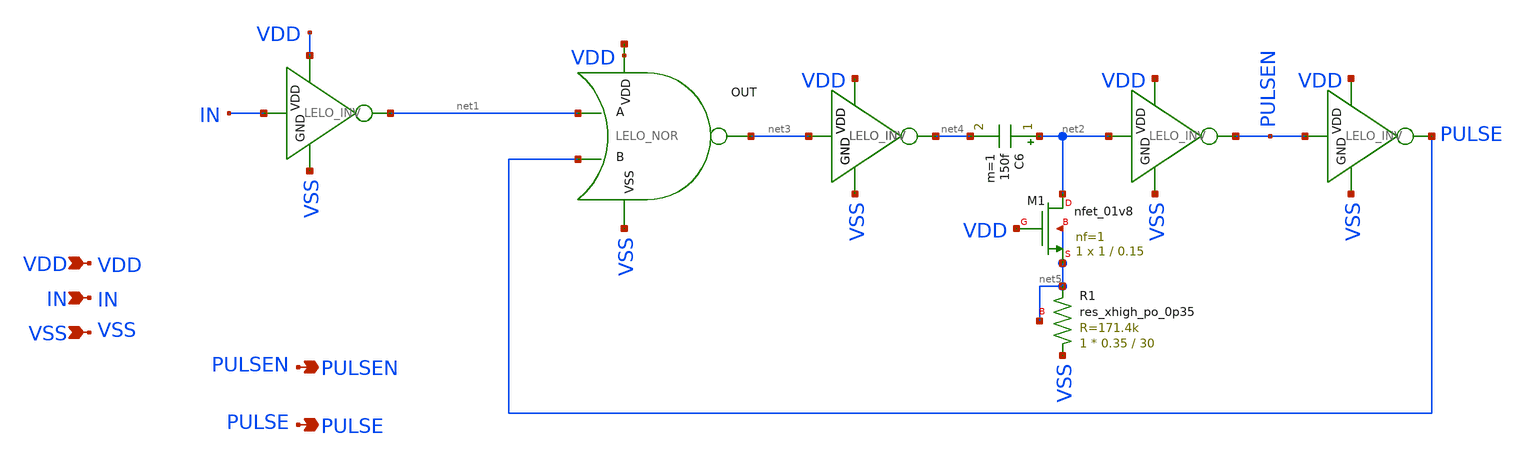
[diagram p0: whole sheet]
** sch_path: design/LELO_SVOD_SKY130A/LELO_ONESHOT.sch
**.subckt LELO_ONESHOT VDD IN VSS PULSEN PULSE
*.ipin VDD
*.ipin IN
*.ipin VSS
*.opin PULSEN
*.opin PULSE
x8 VDD PULSEN PULSE VSS LELO_INV
x12 net6 net3 net1 PULSE VSS LELO_NOR
C6 net2 net4 150f m=1
x13 VDD net2 PULSEN VSS LELO_INV
x18 VDD IN net1 VSS LELO_INV
x1 VDD net3 net4 VSS LELO_INV
XM1 net2 VDD net5 net5 sky130_fd_pr__nfet_01v8 L=0.15 W=1 nf=1 ad='int((1 + 1)/2) * 1 / 1 * 0.29' as='int((1 + 2)/2) * 1 / 1 * 0.29'
+ pd='2*int((1 + 1)/2) * (1 / 1 + 0.29)' ps='2*int((1 + 2)/2) * (1 / 1 + 0.29)' nrd='0.29 / 1 ' nrs='0.29 / 1 '
+ sa=0 sb=0 sd=0 mult=1 m=1
x2 VDD net3 net4 VSS LELO_INV
XR1 VSS net5 net5 sky130_fd_pr__res_xhigh_po_0p35 L=30 mult=1 m=1
**.ends

* expanding   symbol:  LELO_SVOD_SKY130A/LELO_INV.sym # of pins=4
** sym_path: design/LELO_SVOD_SKY130A/LELO_INV.sym
** sch_path: design/LELO_SVOD_SKY130A/LELO_INV.sch
.subckt LELO_INV VDD VIN VOUT GND
*.ipin VIN
*.ipin VDD
*.ipin GND
*.opin VOUT
XM1 VOUT VIN GND GND sky130_fd_pr__nfet_01v8_lvt L=0.15 W=1 nf=1 ad='int((1 + 1)/2) * 1 / 1 * 0.29' as='int((1 + 2)/2) * 1 / 1 * 0.29'
+ pd='2*int((1 + 1)/2) * (1 / 1 + 0.29)' ps='2*int((1 + 2)/2) * (1 / 1 + 0.29)' nrd='0.29 / 1 ' nrs='0.29 / 1 '
+ sa=0 sb=0 sd=0 mult=1 m=1
XM2 VOUT VIN VDD VDD sky130_fd_pr__pfet_01v8_lvt L=0.35 W=1 nf=1 ad='int((1 + 1)/2) * 1 / 1 * 0.29' as='int((1 + 2)/2) * 1 / 1 * 0.29'
+ pd='2*int((1 + 1)/2) * (1 / 1 + 0.29)' ps='2*int((1 + 2)/2) * (1 / 1 + 0.29)' nrd='0.29 / 1 ' nrs='0.29 / 1 '
+ sa=0 sb=0 sd=0 mult=2 m=2
.ends


* expanding   symbol:  LELO_SVOD_SKY130A/LELO_NOR.sym # of pins=5
** sym_path: design/LELO_SVOD_SKY130A/LELO_NOR.sym
** sch_path: design/LELO_SVOD_SKY130A/LELO_NOR.sch
.subckt LELO_NOR VDD OUT A B VSS
*.ipin VDD
*.ipin VSS
*.opin OUT
*.ipin A
*.ipin B
XM2 OUT B VSS VSS sky130_fd_pr__nfet_01v8 L=0.15 W=2 nf=1 ad='int((1 + 1)/2) * 2 / 1 * 0.29' as='int((1 + 2)/2) * 2 / 1 * 0.29'
+ pd='2*int((1 + 1)/2) * (2 / 1 + 0.29)' ps='2*int((1 + 2)/2) * (2 / 1 + 0.29)' nrd='0.29 / 2 ' nrs='0.29 / 2 '
+ sa=0 sb=0 sd=0 mult=1 m=1
XM1 OUT A VSS VSS sky130_fd_pr__nfet_01v8 L=0.15 W=2 nf=1 ad='int((1 + 1)/2) * 2 / 1 * 0.29' as='int((1 + 2)/2) * 2 / 1 * 0.29'
+ pd='2*int((1 + 1)/2) * (2 / 1 + 0.29)' ps='2*int((1 + 2)/2) * (2 / 1 + 0.29)' nrd='0.29 / 2 ' nrs='0.29 / 2 '
+ sa=0 sb=0 sd=0 mult=1 m=1
XM3 OUT B net1 VDD sky130_fd_pr__pfet_01v8 L=0.15 W=4 nf=1 ad='int((1 + 1)/2) * 4 / 1 * 0.29' as='int((1 + 2)/2) * 4 / 1 * 0.29'
+ pd='2*int((1 + 1)/2) * (4 / 1 + 0.29)' ps='2*int((1 + 2)/2) * (4 / 1 + 0.29)' nrd='0.29 / 4 ' nrs='0.29 / 4 '
+ sa=0 sb=0 sd=0 mult=1 m=1
XM4 net1 A VDD VDD sky130_fd_pr__pfet_01v8 L=0.15 W=4 nf=1 ad='int((1 + 1)/2) * 4 / 1 * 0.29' as='int((1 + 2)/2) * 4 / 1 * 0.29'
+ pd='2*int((1 + 1)/2) * (4 / 1 + 0.29)' ps='2*int((1 + 2)/2) * (4 / 1 + 0.29)' nrd='0.29 / 4 ' nrs='0.29 / 4 '
+ sa=0 sb=0 sd=0 mult=1 m=1
.ends

.end
